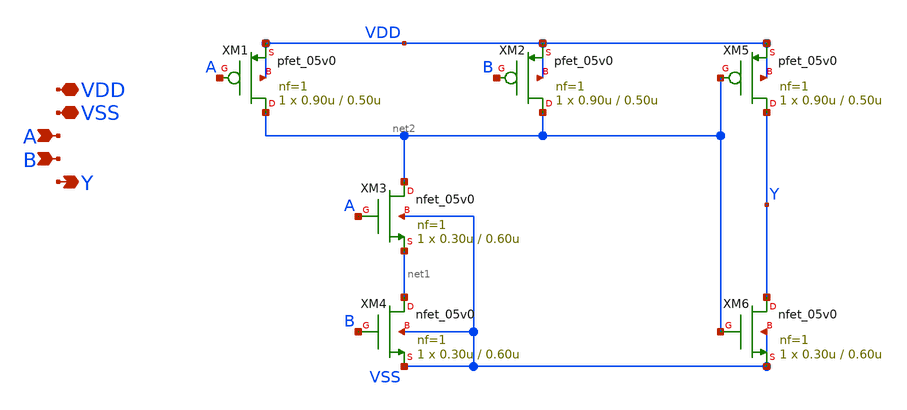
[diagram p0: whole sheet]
** sch_path: xschem/switch-matrix/and2_1.sch
**.subckt and2_1 VDD VSS A B Y
*.iopin VDD
*.iopin VSS
*.ipin A
*.ipin B
*.opin Y
XM1 net2 A VDD VDD pfet_05v0 L=0.50u W=0.90u nf=1 ad='int((nf+1)/2) * W/nf * 0.18u' as='int((nf+2)/2) * W/nf * 0.18u'
+ pd='2*int((nf+1)/2) * (W/nf + 0.18u)' ps='2*int((nf+2)/2) * (W/nf + 0.18u)' nrd='0.18u / W' nrs='0.18u / W'
+ sa=0 sb=0 sd=0 m=1
XM2 net2 B VDD VDD pfet_05v0 L=0.50u W=0.90u nf=1 ad='int((nf+1)/2) * W/nf * 0.18u' as='int((nf+2)/2) * W/nf * 0.18u'
+ pd='2*int((nf+1)/2) * (W/nf + 0.18u)' ps='2*int((nf+2)/2) * (W/nf + 0.18u)' nrd='0.18u / W' nrs='0.18u / W'
+ sa=0 sb=0 sd=0 m=1
XM3 net2 A net1 VSS nfet_05v0 L=0.60u W=0.30u nf=1 ad='int((nf+1)/2) * W/nf * 0.18u' as='int((nf+2)/2) * W/nf * 0.18u'
+ pd='2*int((nf+1)/2) * (W/nf + 0.18u)' ps='2*int((nf+2)/2) * (W/nf + 0.18u)' nrd='0.18u / W' nrs='0.18u / W'
+ sa=0 sb=0 sd=0 m=1
XM4 net1 B VSS VSS nfet_05v0 L=0.60u W=0.30u nf=1 ad='int((nf+1)/2) * W/nf * 0.18u' as='int((nf+2)/2) * W/nf * 0.18u'
+ pd='2*int((nf+1)/2) * (W/nf + 0.18u)' ps='2*int((nf+2)/2) * (W/nf + 0.18u)' nrd='0.18u / W' nrs='0.18u / W'
+ sa=0 sb=0 sd=0 m=1
XM5 Y net2 VDD VDD pfet_05v0 L=0.50u W=0.90u nf=1 ad='int((nf+1)/2) * W/nf * 0.18u' as='int((nf+2)/2) * W/nf * 0.18u'
+ pd='2*int((nf+1)/2) * (W/nf + 0.18u)' ps='2*int((nf+2)/2) * (W/nf + 0.18u)' nrd='0.18u / W' nrs='0.18u / W'
+ sa=0 sb=0 sd=0 m=1
XM6 Y net2 VSS VSS nfet_05v0 L=0.60u W=0.30u nf=1 ad='int((nf+1)/2) * W/nf * 0.18u' as='int((nf+2)/2) * W/nf * 0.18u'
+ pd='2*int((nf+1)/2) * (W/nf + 0.18u)' ps='2*int((nf+2)/2) * (W/nf + 0.18u)' nrd='0.18u / W' nrs='0.18u / W'
+ sa=0 sb=0 sd=0 m=1
**.ends
.end
